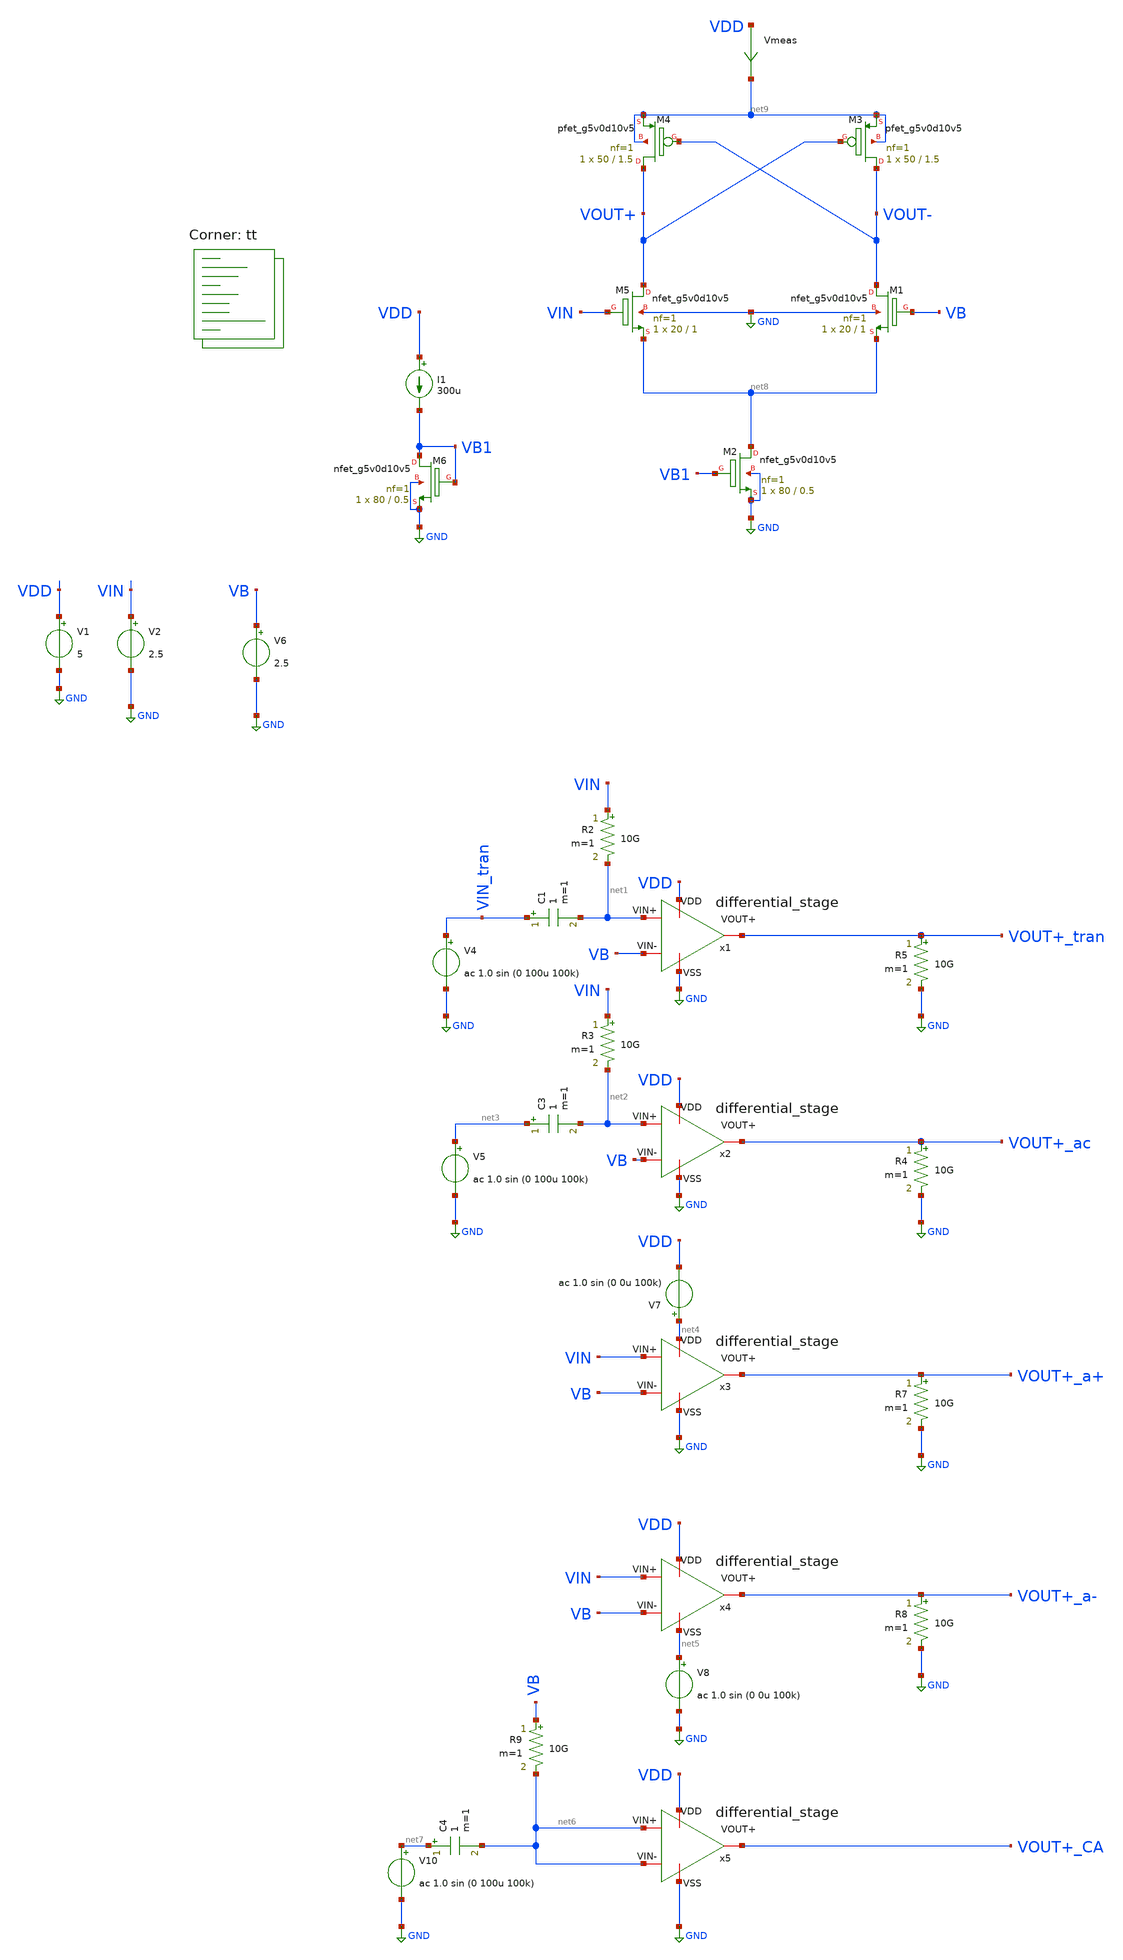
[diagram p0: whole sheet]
** sch_path: old stuff/amplifiers/differencial_stage_amps/stange stages/cross_PMOS/diferential_stage.sch
**.subckt diferential_stage
Vmeas VDD net9 0
.save i(vmeas)
V1 VDD GND 5
V2 VIN GND 2.5
V6 VB GND 2.5
R5 VOUT+_tran GND 10G m=1
R2 VIN net1 10G m=1
V4 VIN_tran GND ac 1.0 sin (0 100u 100k)
C1 VIN_tran net1 1 m=1
R3 VIN net2 10G m=1
C3 net3 net2 1 m=1
V5 net3 GND ac 1.0 sin (0 100u 100k)
R4 VOUT+_ac GND 10G m=1
V7 net4 VDD ac 1.0 sin (0 0u 100k)
R7 VOUT+_a+ GND 10G m=1
V8 net5 GND ac 1.0 sin (0 0u 100k)
R8 VOUT+_a- GND 10G m=1
R9 VB net6 10G m=1
C4 net7 net6 1 m=1
V10 net7 GND ac 1.0 sin (0 100u 100k)
x1 VDD GND net1 VB VOUT+_tran differential_stage
x2 VDD GND net2 VB VOUT+_ac differential_stage
x3 net4 GND VIN VB VOUT+_a+ differential_stage
x4 VDD net5 VIN VB VOUT+_a- differential_stage
x5 VDD GND net6 net6 VOUT+_CA differential_stage
XM5 VOUT+ VIN net8 GND sky130_fd_pr__nfet_g5v0d10v5 L=1 W=20 nf=1 ad='int((1 + 1)/2) * 20 / 1 * 0.29'
+ as='int((1 + 2)/2) * 20 / 1 * 0.29' pd='2*int((1 + 1)/2) * (20 / 1 + 0.29)' ps='2*int((1 + 2)/2) * (20 / 1 + 0.29)'
+ nrd='0.29 / 20 ' nrs='0.29 / 20 ' sa=0 sb=0 sd=0 mult=1 m=1
XM1 VOUT- VB net8 GND sky130_fd_pr__nfet_g5v0d10v5 L=1 W=20 nf=1 ad='int((1 + 1)/2) * 20 / 1 * 0.29'
+ as='int((1 + 2)/2) * 20 / 1 * 0.29' pd='2*int((1 + 1)/2) * (20 / 1 + 0.29)' ps='2*int((1 + 2)/2) * (20 / 1 + 0.29)'
+ nrd='0.29 / 20 ' nrs='0.29 / 20 ' sa=0 sb=0 sd=0 mult=1 m=1
XM4 VOUT+ VOUT- net9 net9 sky130_fd_pr__pfet_g5v0d10v5 L=1.5 W=50 nf=1 ad='int((1 + 1)/2) * 50 / 1 * 0.29'
+ as='int((1 + 2)/2) * 50 / 1 * 0.29' pd='2*int((1 + 1)/2) * (50 / 1 + 0.29)' ps='2*int((1 + 2)/2) * (50 / 1 + 0.29)'
+ nrd='0.29 / 50 ' nrs='0.29 / 50 ' sa=0 sb=0 sd=0 mult=1 m=1
I1 VDD VB1 300u
XM6 VB1 VB1 GND GND sky130_fd_pr__nfet_g5v0d10v5 L=0.5 W=80 nf=1 ad='int((1 + 1)/2) * 80 / 1 * 0.29'
+ as='int((1 + 2)/2) * 80 / 1 * 0.29' pd='2*int((1 + 1)/2) * (80 / 1 + 0.29)' ps='2*int((1 + 2)/2) * (80 / 1 + 0.29)'
+ nrd='0.29 / 80 ' nrs='0.29 / 80 ' sa=0 sb=0 sd=0 mult=1 m=1
XM3 VOUT- VOUT+ net9 net9 sky130_fd_pr__pfet_g5v0d10v5 L=1.5 W=50 nf=1 ad='int((1 + 1)/2) * 50 / 1 * 0.29'
+ as='int((1 + 2)/2) * 50 / 1 * 0.29' pd='2*int((1 + 1)/2) * (50 / 1 + 0.29)' ps='2*int((1 + 2)/2) * (50 / 1 + 0.29)'
+ nrd='0.29 / 50 ' nrs='0.29 / 50 ' sa=0 sb=0 sd=0 mult=1 m=1
XM2 net8 VB1 GND GND sky130_fd_pr__nfet_g5v0d10v5 L=0.5 W=80 nf=1 ad='int((1 + 1)/2) * 80 / 1 * 0.29'
+ as='int((1 + 2)/2) * 80 / 1 * 0.29' pd='2*int((1 + 1)/2) * (80 / 1 + 0.29)' ps='2*int((1 + 2)/2) * (80 / 1 + 0.29)'
+ nrd='0.29 / 80 ' nrs='0.29 / 80 ' sa=0 sb=0 sd=0 mult=1 m=1
**** begin user architecture code

**************************************************************
**************************************************************
**************************************************************
**************************************************************
**************************************************************
*LIBs*********************************************************
**************************************************************
**************************************************************
**************************************************************
**************************************************************
**************************************************************
*.lib $::SKYWATER_MODELS/sky130.lib.spice tt
* chose the corners in the corner file
* tt_mm for mismatch
* ss ff sf fs standart corners
* ll hh lh hl capacitor and resistors corners
* mc for total process variation including corners
**************************************************************
**************************************************************
**************************************************************
**************************************************************
**************************************************************
*Corners/montecarlo options***********************************
**************************************************************
**************************************************************
**************************************************************
**************************************************************
**************************************************************
.TEMP 27
**************************************************************
**************************************************************
**************************************************************
**************************************************************
*SIMULATION and Plots*****************************************
**************************************************************
**************************************************************
**************************************************************
**************************************************************
.control
save all
dc V2 0 5 0.01
*dc simulation
plot v(VOUT-) v(VIN) deriv(v(VOUT-)) v(VOUT+) deriv(v(VOUT+))
*ploting VIN VOUT and the voltage gain
plot i(Vmeas)
plot -i(v1)
*ploting the current for curiosity
tran 1ns 20u
*transient simulation
plot (v(VOUT+_tran))
*simple plot to exemplify the gain
fft v(VOUT+_tran) v(VIN_tran)
*fast fourier transfor
plot mag(v(VOUT+_tran)) mag(v(VIN_tran))
ac dec 20 1 1000G
*simple ac simulation
plot db(v(VOUT+_ac))
plot db(v(VOUT+_a+))
plot db(v(VOUT+_a-))
plot db(v(VOUT+_CA))
plot db((v(VOUT+_ac))/(v(VOUT+_CA)))
plot db((v(VOUT+_ac))/(v(VOUT+_a+)))
plot db((v(VOUT+_ac))/(v(VOUT+_a-)))
.endc

.lib $::SKYWATER_MODELS/sky130.lib.spice tt
**** end user architecture code
**.ends
.GLOBAL GND
.end
